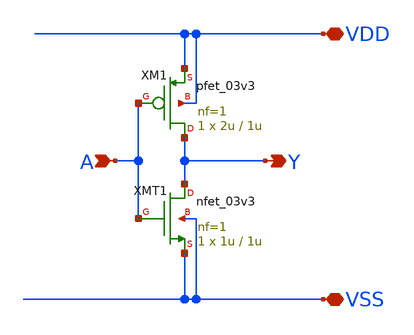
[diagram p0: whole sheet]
** sch_path: comparator_alt/schematic/inv_slow.sch
**.subckt inv_slow VDD VSS Y A
*.iopin VDD
*.iopin VSS
*.opin Y
*.ipin A
XMT1 Y A VSS VSS nfet_03v3 L=1u W=1u nf=1 ad='int((nf+1)/2) * W/nf * 0.18u' as='int((nf+2)/2) * W/nf * 0.18u'
+ pd='2*int((nf+1)/2) * (W/nf + 0.18u)' ps='2*int((nf+2)/2) * (W/nf + 0.18u)' nrd='0.18u / W' nrs='0.18u / W'
+ sa=0 sb=0 sd=0 m=1
XM1 Y A VDD VDD pfet_03v3 L=1u W=2u nf=1 ad='int((nf+1)/2) * W/nf * 0.18u' as='int((nf+2)/2) * W/nf * 0.18u'
+ pd='2*int((nf+1)/2) * (W/nf + 0.18u)' ps='2*int((nf+2)/2) * (W/nf + 0.18u)' nrd='0.18u / W' nrs='0.18u / W'
+ sa=0 sb=0 sd=0 m=1
**.ends
.end
